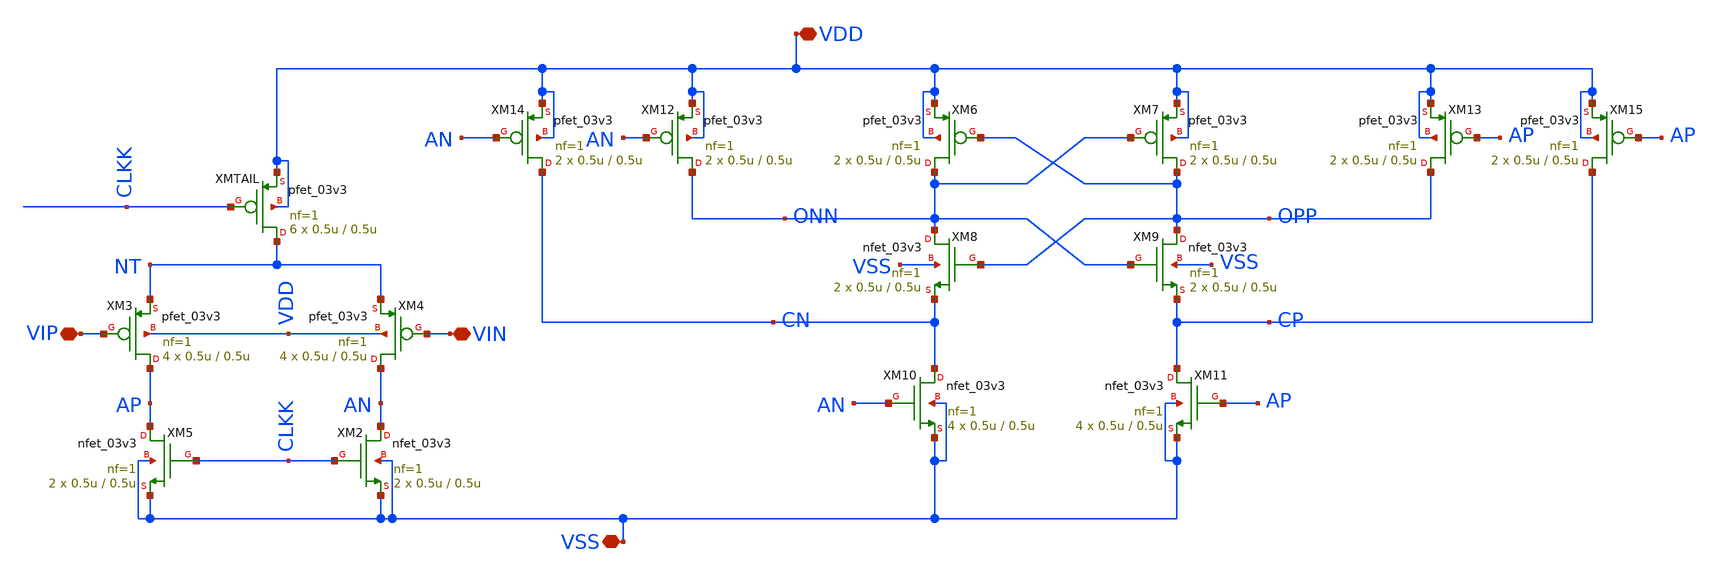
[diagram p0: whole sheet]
** sch_path: designs/sar_adc/comparator/StrongARM/xschem/strongARM_sb.sch
**.subckt strongARM_sb VSS VDD VIN VIP
*.iopin VSS
*.iopin VDD
*.iopin VIN
*.iopin VIP
XMTAIL NT CLKK VDD VDD pfet_03v3 L=0.5u W=0.5u nf=1 ad='int((nf+1)/2) * W/nf * 0.18u' as='int((nf+2)/2) * W/nf * 0.18u'
+ pd='2*int((nf+1)/2) * (W/nf + 0.18u)' ps='2*int((nf+2)/2) * (W/nf + 0.18u)' nrd='0.18u / W' nrs='0.18u / W'
+ sa=0 sb=0 sd=0 m=6
XM2 AN CLKK VSS VSS nfet_03v3 L=0.5u W=0.5u nf=1 ad='int((nf+1)/2) * W/nf * 0.18u' as='int((nf+2)/2) * W/nf * 0.18u'
+ pd='2*int((nf+1)/2) * (W/nf + 0.18u)' ps='2*int((nf+2)/2) * (W/nf + 0.18u)' nrd='0.18u / W' nrs='0.18u / W'
+ sa=0 sb=0 sd=0 m=2
XM3 AP VIP NT VDD pfet_03v3 L=0.5u W=0.5u nf=1 ad='int((nf+1)/2) * W/nf * 0.18u' as='int((nf+2)/2) * W/nf * 0.18u'
+ pd='2*int((nf+1)/2) * (W/nf + 0.18u)' ps='2*int((nf+2)/2) * (W/nf + 0.18u)' nrd='0.18u / W' nrs='0.18u / W'
+ sa=0 sb=0 sd=0 m=4
XM4 AN VIN NT VDD pfet_03v3 L=0.5u W=0.5u nf=1 ad='int((nf+1)/2) * W/nf * 0.18u' as='int((nf+2)/2) * W/nf * 0.18u'
+ pd='2*int((nf+1)/2) * (W/nf + 0.18u)' ps='2*int((nf+2)/2) * (W/nf + 0.18u)' nrd='0.18u / W' nrs='0.18u / W'
+ sa=0 sb=0 sd=0 m=4
XM5 AP CLKK VSS VSS nfet_03v3 L=0.5u W=0.5u nf=1 ad='int((nf+1)/2) * W/nf * 0.18u' as='int((nf+2)/2) * W/nf * 0.18u'
+ pd='2*int((nf+1)/2) * (W/nf + 0.18u)' ps='2*int((nf+2)/2) * (W/nf + 0.18u)' nrd='0.18u / W' nrs='0.18u / W'
+ sa=0 sb=0 sd=0 m=2
XM6 ONN OPP VDD VDD pfet_03v3 L=0.5u W=0.5u nf=1 ad='int((nf+1)/2) * W/nf * 0.18u' as='int((nf+2)/2) * W/nf * 0.18u'
+ pd='2*int((nf+1)/2) * (W/nf + 0.18u)' ps='2*int((nf+2)/2) * (W/nf + 0.18u)' nrd='0.18u / W' nrs='0.18u / W'
+ sa=0 sb=0 sd=0 m=2
XM7 OPP ONN VDD VDD pfet_03v3 L=0.5u W=0.5u nf=1 ad='int((nf+1)/2) * W/nf * 0.18u' as='int((nf+2)/2) * W/nf * 0.18u'
+ pd='2*int((nf+1)/2) * (W/nf + 0.18u)' ps='2*int((nf+2)/2) * (W/nf + 0.18u)' nrd='0.18u / W' nrs='0.18u / W'
+ sa=0 sb=0 sd=0 m=2
XM8 ONN OPP CN VSS nfet_03v3 L=0.5u W=0.5u nf=1 ad='int((nf+1)/2) * W/nf * 0.18u' as='int((nf+2)/2) * W/nf * 0.18u'
+ pd='2*int((nf+1)/2) * (W/nf + 0.18u)' ps='2*int((nf+2)/2) * (W/nf + 0.18u)' nrd='0.18u / W' nrs='0.18u / W'
+ sa=0 sb=0 sd=0 m=2
XM9 OPP ONN CP VSS nfet_03v3 L=0.5u W=0.5u nf=1 ad='int((nf+1)/2) * W/nf * 0.18u' as='int((nf+2)/2) * W/nf * 0.18u'
+ pd='2*int((nf+1)/2) * (W/nf + 0.18u)' ps='2*int((nf+2)/2) * (W/nf + 0.18u)' nrd='0.18u / W' nrs='0.18u / W'
+ sa=0 sb=0 sd=0 m=2
XM10 CN AN VSS VSS nfet_03v3 L=0.5u W=0.5u nf=1 ad='int((nf+1)/2) * W/nf * 0.18u' as='int((nf+2)/2) * W/nf * 0.18u'
+ pd='2*int((nf+1)/2) * (W/nf + 0.18u)' ps='2*int((nf+2)/2) * (W/nf + 0.18u)' nrd='0.18u / W' nrs='0.18u / W'
+ sa=0 sb=0 sd=0 m=4
XM11 CP AP VSS VSS nfet_03v3 L=0.5u W=0.5u nf=1 ad='int((nf+1)/2) * W/nf * 0.18u' as='int((nf+2)/2) * W/nf * 0.18u'
+ pd='2*int((nf+1)/2) * (W/nf + 0.18u)' ps='2*int((nf+2)/2) * (W/nf + 0.18u)' nrd='0.18u / W' nrs='0.18u / W'
+ sa=0 sb=0 sd=0 m=4
XM12 ONN AN VDD VDD pfet_03v3 L=0.5u W=0.5u nf=1 ad='int((nf+1)/2) * W/nf * 0.18u' as='int((nf+2)/2) * W/nf * 0.18u'
+ pd='2*int((nf+1)/2) * (W/nf + 0.18u)' ps='2*int((nf+2)/2) * (W/nf + 0.18u)' nrd='0.18u / W' nrs='0.18u / W'
+ sa=0 sb=0 sd=0 m=2
XM13 OPP AP VDD VDD pfet_03v3 L=0.5u W=0.5u nf=1 ad='int((nf+1)/2) * W/nf * 0.18u' as='int((nf+2)/2) * W/nf * 0.18u'
+ pd='2*int((nf+1)/2) * (W/nf + 0.18u)' ps='2*int((nf+2)/2) * (W/nf + 0.18u)' nrd='0.18u / W' nrs='0.18u / W'
+ sa=0 sb=0 sd=0 m=2
XM14 CN AN VDD VDD pfet_03v3 L=0.5u W=0.5u nf=1 ad='int((nf+1)/2) * W/nf * 0.18u' as='int((nf+2)/2) * W/nf * 0.18u'
+ pd='2*int((nf+1)/2) * (W/nf + 0.18u)' ps='2*int((nf+2)/2) * (W/nf + 0.18u)' nrd='0.18u / W' nrs='0.18u / W'
+ sa=0 sb=0 sd=0 m=2
XM15 CP AP VDD VDD pfet_03v3 L=0.5u W=0.5u nf=1 ad='int((nf+1)/2) * W/nf * 0.18u' as='int((nf+2)/2) * W/nf * 0.18u'
+ pd='2*int((nf+1)/2) * (W/nf + 0.18u)' ps='2*int((nf+2)/2) * (W/nf + 0.18u)' nrd='0.18u / W' nrs='0.18u / W'
+ sa=0 sb=0 sd=0 m=2
**.ends
.end
